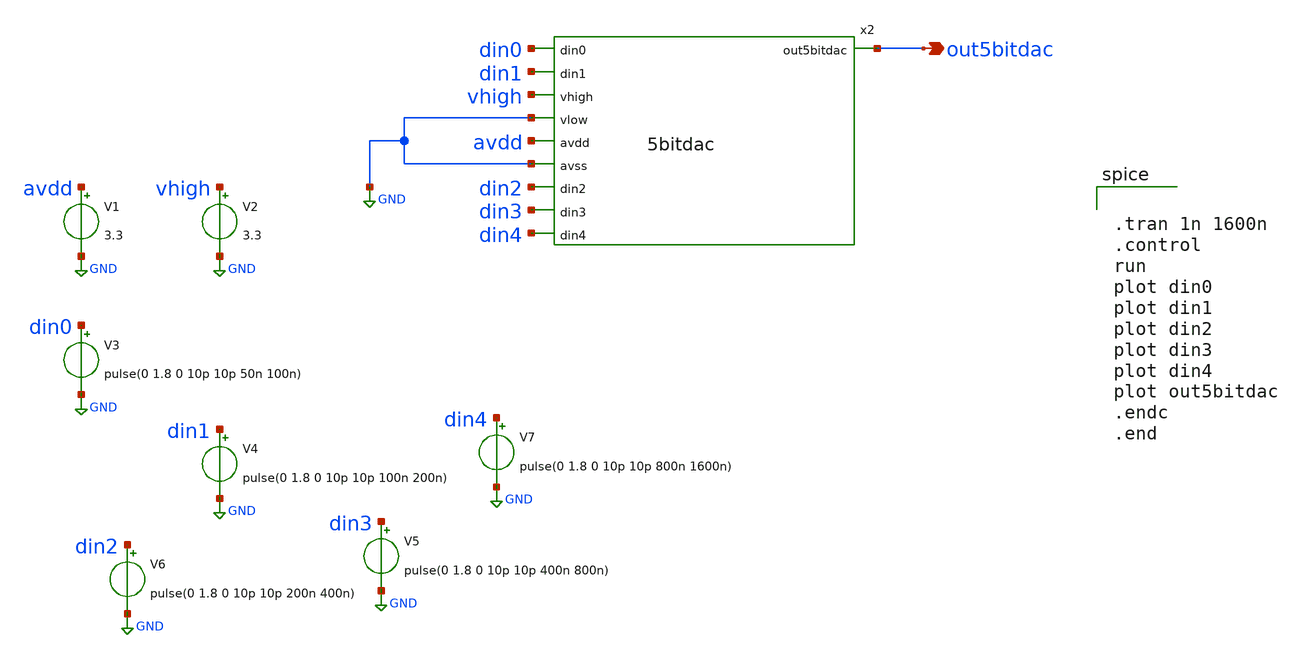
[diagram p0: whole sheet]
** sch_path: xschem/tb_5bitdac.sch
**.subckt tb_5bitdac out5bitdac
*.opin out5bitdac
V1 avdd GND 3.3
V2 vhigh GND 3.3
V3 din0 GND pulse(0 1.8 0 10p 10p 50n 100n)
V4 din1 GND pulse(0 1.8 0 10p 10p 100n 200n)
V5 din3 GND pulse(0 1.8 0 10p 10p 400n 800n)
V6 din2 GND pulse(0 1.8 0 10p 10p 200n 400n)
V7 din4 GND pulse(0 1.8 0 10p 10p 800n 1600n)
x2 out5bitdac din0 din1 vhigh GND avdd GND din2 din3 din4 5bitdac
**** begin user architecture code

** opencircuitdesign pdks install
.lib $::SKYWATER_MODELS/sky130.lib.spice tt




.tran 1n 1600n
.control
run
plot din0
plot din1
plot din2
plot din3
plot din4
plot out5bitdac
.endc
.end

**** end user architecture code
**.ends

* expanding   symbol:  5bitdac.sym # of pins=10
** sym_path: xschem/5bitdac.sym
** sch_path: xschem/5bitdac.sch
.subckt 5bitdac out5bitdac din0 din1 vhigh vlow avdd avss din2 din3 din4
*.ipin din0
*.ipin din1
*.ipin vhigh
*.ipin vlow
*.ipin avdd
*.ipin avss
*.ipin din2
*.ipin din3
*.opin out5bitdac
*.ipin din4
x1 x1out din0 din1 vhigh net2 avdd avss din2 din3 4bitdac
x2 x2out din0 din1 net1 vlow avdd avss din2 din3 4bitdac
x3 out5bitdac x1out x2out avss avdd din4 switch
XR6 net1 net2 avss sky130_fd_pr__res_high_po_0p35 L=3 mult=1 m=1
.ends


* expanding   symbol:  4bitdac.sym # of pins=9
** sym_path: xschem/4bitdac.sym
** sch_path: xschem/4bitdac.sch
.subckt 4bitdac out4bitdac din0 din1 vhigh vlow avdd avss din2 din3
*.ipin din0
*.ipin din1
*.ipin vhigh
*.ipin vlow
*.ipin avdd
*.ipin avss
*.ipin din2
*.ipin din3
*.opin out4bitdac
x1 x1out din0 din1 vhigh net1 avdd avss din2 3bitdac
x2 x2out din0 din1 net2 vlow avdd avss din2 3bitdac
x3 out4bitdac x1out x2out avss avdd din3 switch
XR6 net2 net1 avss sky130_fd_pr__res_high_po_0p35 L=3 mult=1 m=1
.ends


* expanding   symbol:  switch.sym # of pins=6
** sym_path: xschem/switch.sym
** sch_path: xschem/switch.sch
.subckt switch outsw in1 in2 avss avdd din
*.ipin avss
*.ipin avdd
*.ipin din
*.ipin in1
*.ipin in2
*.opin outsw
XM11 dinbar din avdd avdd sky130_fd_pr__pfet_01v8 L=0.15 W=1.2 nf=1 ad='int((nf+1)/2) * W/nf * 0.29'
+ as='int((nf+2)/2) * W/nf * 0.29' pd='2*int((nf+1)/2) * (W/nf + 0.29)' ps='2*int((nf+2)/2) * (W/nf + 0.29)'
+ nrd='0.29 / W' nrs='0.29 / W' sa=0 sb=0 sd=0 mult=1 m=1
XM1 wc dinbar avdd avdd sky130_fd_pr__pfet_01v8 L=0.15 W=1.2 nf=1 ad='int((nf+1)/2) * W/nf * 0.29' as='int((nf+2)/2) * W/nf * 0.29'
+ pd='2*int((nf+1)/2) * (W/nf + 0.29)' ps='2*int((nf+2)/2) * (W/nf + 0.29)' nrd='0.29 / W' nrs='0.29 / W'
+ sa=0 sb=0 sd=0 mult=1 m=1
XM2 dinbar din avss avss sky130_fd_pr__nfet_01v8 L=0.15 W=0.6 nf=1 ad='int((1 + 1)/2) * 0.6 / 1 * 0.29'
+ as='int((1 + 2)/2) * 0.6 / 1 * 0.29' pd='2*int((1 + 1)/2) * (0.6 / 1 + 0.29)' ps='2*int((1 + 2)/2) * (0.6 / 1 + 0.29)'
+ nrd='0.29 / 0.6 ' nrs='0.29 / 0.6 ' sa=0 sb=0 sd=0 mult=1 m=1
XM3 wc dinbar avss avss sky130_fd_pr__nfet_01v8 L=0.15 W=0.6 nf=1 ad='int((1 + 1)/2) * 0.6 / 1 * 0.29'
+ as='int((1 + 2)/2) * 0.6 / 1 * 0.29' pd='2*int((1 + 1)/2) * (0.6 / 1 + 0.29)' ps='2*int((1 + 2)/2) * (0.6 / 1 + 0.29)'
+ nrd='0.29 / 0.6 ' nrs='0.29 / 0.6 ' sa=0 sb=0 sd=0 mult=1 m=1
XM4 outsw dinbar in1 avdd sky130_fd_pr__pfet_01v8 L=0.15 W=1.2 nf=1 ad='int((nf+1)/2) * W/nf * 0.29'
+ as='int((nf+2)/2) * W/nf * 0.29' pd='2*int((nf+1)/2) * (W/nf + 0.29)' ps='2*int((nf+2)/2) * (W/nf + 0.29)'
+ nrd='0.29 / W' nrs='0.29 / W' sa=0 sb=0 sd=0 mult=1 m=1
XM5 outsw dinbar in2 avss sky130_fd_pr__nfet_01v8 L=0.15 W=0.6 nf=1 ad='int((1 + 1)/2) * 0.6 / 1 * 0.29'
+ as='int((1 + 2)/2) * 0.6 / 1 * 0.29' pd='2*int((1 + 1)/2) * (0.6 / 1 + 0.29)' ps='2*int((1 + 2)/2) * (0.6 / 1 + 0.29)'
+ nrd='0.29 / 0.6 ' nrs='0.29 / 0.6 ' sa=0 sb=0 sd=0 mult=1 m=1
XM6 in1 wc outsw avss sky130_fd_pr__nfet_01v8 L=0.15 W=0.6 nf=1 ad='int((1 + 1)/2) * 0.6 / 1 * 0.29'
+ as='int((1 + 2)/2) * 0.6 / 1 * 0.29' pd='2*int((1 + 1)/2) * (0.6 / 1 + 0.29)' ps='2*int((1 + 2)/2) * (0.6 / 1 + 0.29)'
+ nrd='0.29 / 0.6 ' nrs='0.29 / 0.6 ' sa=0 sb=0 sd=0 mult=1 m=1
XM7 in2 wc outsw avdd sky130_fd_pr__pfet_01v8 L=0.15 W=1.2 nf=1 ad='int((nf+1)/2) * W/nf * 0.29' as='int((nf+2)/2) * W/nf * 0.29'
+ pd='2*int((nf+1)/2) * (W/nf + 0.29)' ps='2*int((nf+2)/2) * (W/nf + 0.29)' nrd='0.29 / W' nrs='0.29 / W'
+ sa=0 sb=0 sd=0 mult=1 m=1
.ends


* expanding   symbol:  3bitdac.sym # of pins=8
** sym_path: xschem/3bitdac.sym
** sch_path: xschem/3bitdac.sch
.subckt 3bitdac out3bitdac din0 din1 vrefh vrefl avdd avss din2
*.ipin din0
*.ipin din1
*.ipin vrefh
*.ipin vrefl
*.ipin avdd
*.ipin avss
*.opin out3bitdac
*.ipin din2
x1 x1out din0 vrefh net1 avdd avss din1 2bitdac
x2 x2out din0 net2 vrefl avdd avss din1 2bitdac
x3 out3bitdac x1out x2out avss avdd din2 switch
XR6 net2 net1 avss sky130_fd_pr__res_high_po_0p35 L=3 mult=1 m=1
.ends


* expanding   symbol:  2bitdac.sym # of pins=7
** sym_path: xschem/2bitdac.sym
** sch_path: xschem/2bitdac.sch
.subckt 2bitdac out2bitdac din0 vhigh vlow avdd avss din1
*.ipin din0
*.ipin vhigh
*.ipin vlow
*.ipin avdd
*.ipin avss
*.ipin din1
*.opin out2bitdac
x1 x1_out net1 net2 avss avdd din0 switch
x2 x2_out net3 vlow avss avdd din0 switch
x3 out2bitdac x1_out x2_out avss avdd din1 switch
XR6 net1 vhigh avss sky130_fd_pr__res_high_po_0p35 L=3 mult=1 m=1
XR1 net2 net1 avss sky130_fd_pr__res_high_po_0p35 L=3 mult=1 m=1
XR2 net3 net2 avss sky130_fd_pr__res_high_po_0p35 L=3 mult=1 m=1
XR3 vlow net3 avss sky130_fd_pr__res_high_po_0p35 L=3 mult=1 m=1
.ends

.GLOBAL GND
.end
